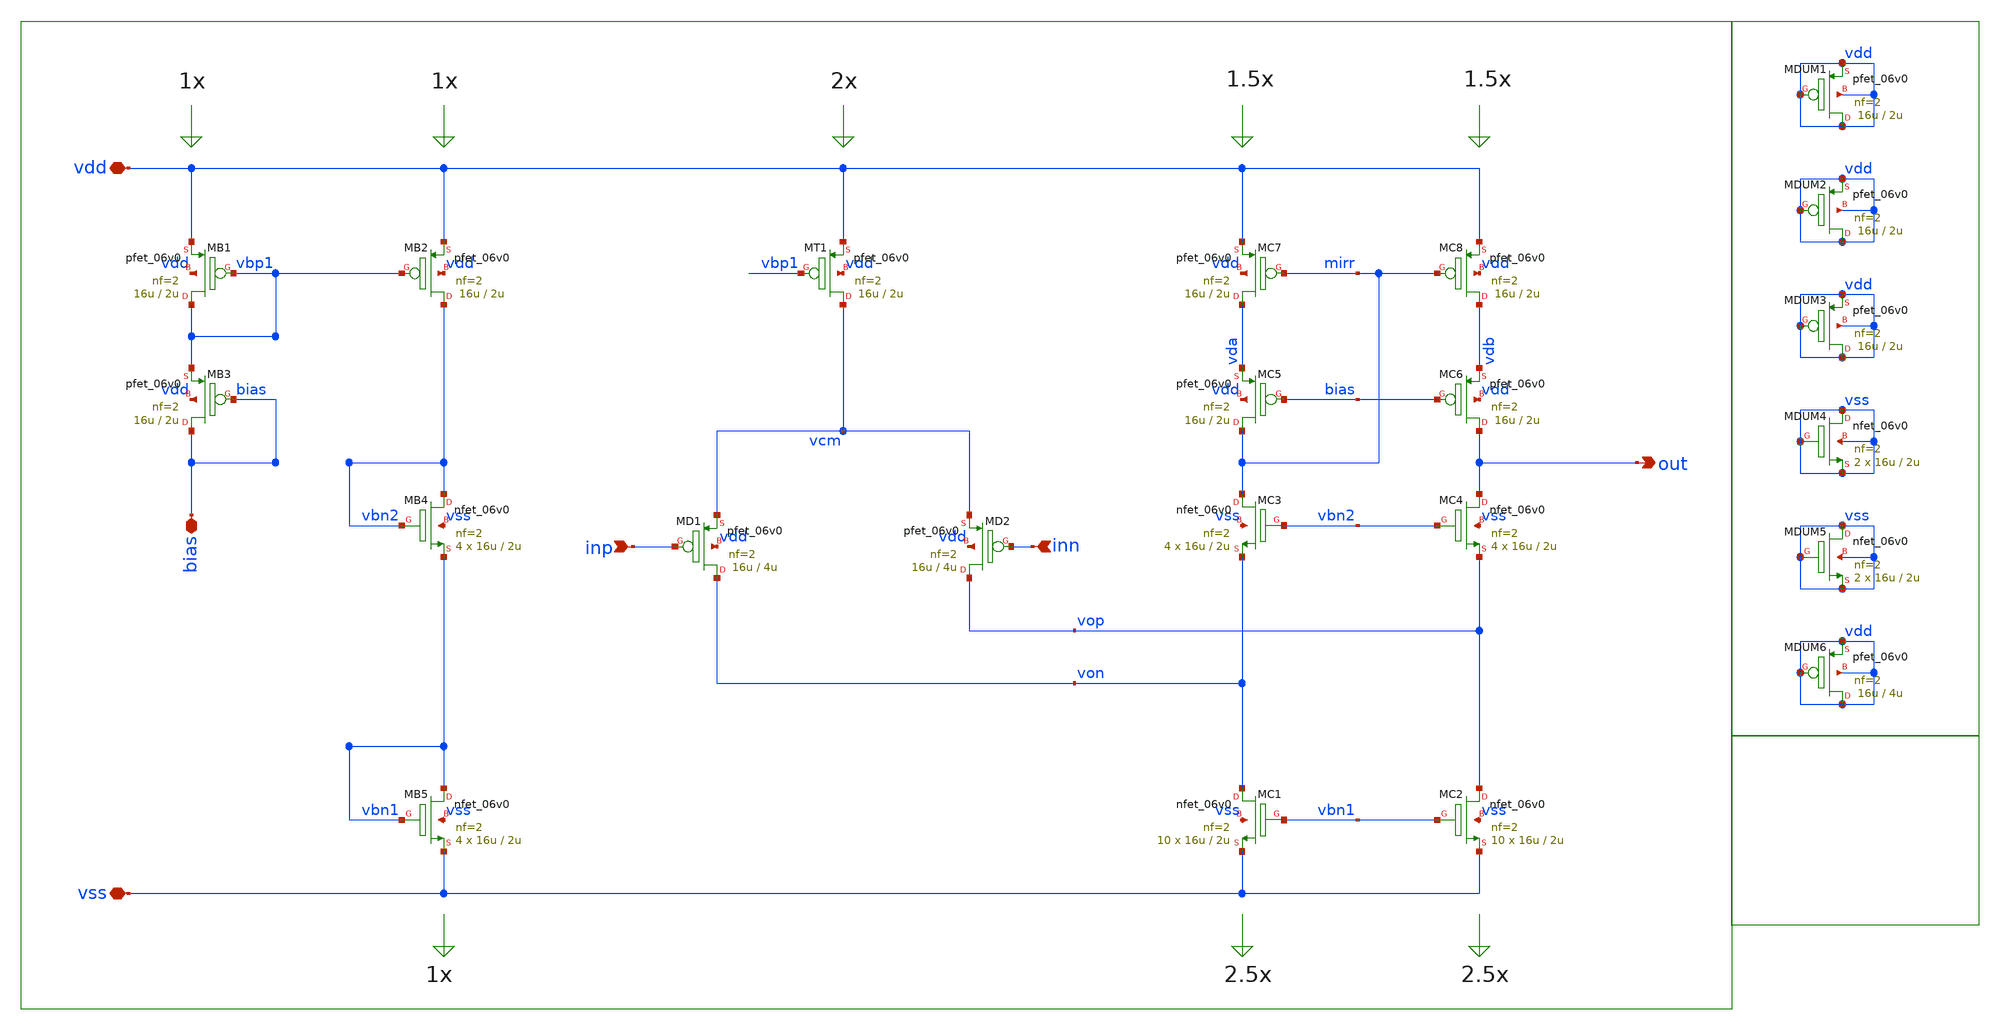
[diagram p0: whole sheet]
** sch_path: xschem/sch/bandgap_cm/bg_amplifier/bg_amplifier.sch
**.subckt bg_amplifier inn inp out bias vdd vss
*.ipin inn
*.ipin inp
*.opin out
*.iopin bias
*.iopin vdd
*.iopin vss
XMB5 vbn1 vbn1 vss vss nfet_06v0 L=2u W=16u nf=2 ad='int((nf+1)/2) * W/nf * 0.18u' as='int((nf+2)/2) * W/nf * 0.18u'
+ pd='2*int((nf+1)/2) * (W/nf + 0.18u)' ps='2*int((nf+2)/2) * (W/nf + 0.18u)' nrd='0.18u / W' nrs='0.18u / W'
+ sa=0 sb=0 sd=0 m=4 par=4
XMC1 von vbn1 vss vss nfet_06v0 L=2u W=16u nf=2 ad='int((nf+1)/2) * W/nf * 0.18u' as='int((nf+2)/2) * W/nf * 0.18u'
+ pd='2*int((nf+1)/2) * (W/nf + 0.18u)' ps='2*int((nf+2)/2) * (W/nf + 0.18u)' nrd='0.18u / W' nrs='0.18u / W'
+ sa=0 sb=0 sd=0 m=10 par=10
XMC2 vop vbn1 vss vss nfet_06v0 L=2u W=16u nf=2 ad='int((nf+1)/2) * W/nf * 0.18u' as='int((nf+2)/2) * W/nf * 0.18u'
+ pd='2*int((nf+1)/2) * (W/nf + 0.18u)' ps='2*int((nf+2)/2) * (W/nf + 0.18u)' nrd='0.18u / W' nrs='0.18u / W'
+ sa=0 sb=0 sd=0 m=10 par=10
XMC3 mirr vbn2 von vss nfet_06v0 L=2u W=16u nf=2 ad='int((nf+1)/2) * W/nf * 0.18u' as='int((nf+2)/2) * W/nf * 0.18u'
+ pd='2*int((nf+1)/2) * (W/nf + 0.18u)' ps='2*int((nf+2)/2) * (W/nf + 0.18u)' nrd='0.18u / W' nrs='0.18u / W'
+ sa=0 sb=0 sd=0 m=4 par=4
XMC4 out vbn2 vop vss nfet_06v0 L=2u W=16u nf=2 ad='int((nf+1)/2) * W/nf * 0.18u' as='int((nf+2)/2) * W/nf * 0.18u'
+ pd='2*int((nf+1)/2) * (W/nf + 0.18u)' ps='2*int((nf+2)/2) * (W/nf + 0.18u)' nrd='0.18u / W' nrs='0.18u / W'
+ sa=0 sb=0 sd=0 m=4 par=4
XMB3 bias bias vbp1 vdd pfet_06v0 L=2u W=16u nf=2 ad='int((nf+1)/2) * W/nf * 0.18u' as='int((nf+2)/2) * W/nf * 0.18u'
+ pd='2*int((nf+1)/2) * (W/nf + 0.18u)' ps='2*int((nf+2)/2) * (W/nf + 0.18u)' nrd='0.18u / W' nrs='0.18u / W'
+ sa=0 sb=0 sd=0 m=2 par=2
XMB1 vbp1 vbp1 vdd vdd pfet_06v0 L=2u W=16u nf=2 ad='int((nf+1)/2) * W/nf * 0.18u' as='int((nf+2)/2) * W/nf * 0.18u'
+ pd='2*int((nf+1)/2) * (W/nf + 0.18u)' ps='2*int((nf+2)/2) * (W/nf + 0.18u)' nrd='0.18u / W' nrs='0.18u / W'
+ sa=0 sb=0 sd=0 m=4 par=4
XMB2 vbn2 vbp1 vdd vdd pfet_06v0 L=2u W=16u nf=2 ad='int((nf+1)/2) * W/nf * 0.18u' as='int((nf+2)/2) * W/nf * 0.18u'
+ pd='2*int((nf+1)/2) * (W/nf + 0.18u)' ps='2*int((nf+2)/2) * (W/nf + 0.18u)' nrd='0.18u / W' nrs='0.18u / W'
+ sa=0 sb=0 sd=0 m=4 par=4
XMT1 vcm vbp1 vdd vdd pfet_06v0 L=2u W=16u nf=2 ad='int((nf+1)/2) * W/nf * 0.18u' as='int((nf+2)/2) * W/nf * 0.18u'
+ pd='2*int((nf+1)/2) * (W/nf + 0.18u)' ps='2*int((nf+2)/2) * (W/nf + 0.18u)' nrd='0.18u / W' nrs='0.18u / W'
+ sa=0 sb=0 sd=0 m=8 par=8
XMD1 von inp vcm vdd pfet_06v0 L=4u W=16u nf=2 ad='int((nf+1)/2) * W/nf * 0.18u' as='int((nf+2)/2) * W/nf * 0.18u'
+ pd='2*int((nf+1)/2) * (W/nf + 0.18u)' ps='2*int((nf+2)/2) * (W/nf + 0.18u)' nrd='0.18u / W' nrs='0.18u / W'
+ sa=0 sb=0 sd=0 m=4 par=4
XMD2 vop inn vcm vdd pfet_06v0 L=4u W=16u nf=2 ad='int((nf+1)/2) * W/nf * 0.18u' as='int((nf+2)/2) * W/nf * 0.18u'
+ pd='2*int((nf+1)/2) * (W/nf + 0.18u)' ps='2*int((nf+2)/2) * (W/nf + 0.18u)' nrd='0.18u / W' nrs='0.18u / W'
+ sa=0 sb=0 sd=0 m=4 par=4
XMC7 vda mirr vdd vdd pfet_06v0 L=2u W=16u nf=2 ad='int((nf+1)/2) * W/nf * 0.18u' as='int((nf+2)/2) * W/nf * 0.18u'
+ pd='2*int((nf+1)/2) * (W/nf + 0.18u)' ps='2*int((nf+2)/2) * (W/nf + 0.18u)' nrd='0.18u / W' nrs='0.18u / W'
+ sa=0 sb=0 sd=0 m=2 par=2
XMC8 vdb mirr vdd vdd pfet_06v0 L=2u W=16u nf=2 ad='int((nf+1)/2) * W/nf * 0.18u' as='int((nf+2)/2) * W/nf * 0.18u'
+ pd='2*int((nf+1)/2) * (W/nf + 0.18u)' ps='2*int((nf+2)/2) * (W/nf + 0.18u)' nrd='0.18u / W' nrs='0.18u / W'
+ sa=0 sb=0 sd=0 m=2 par=2
XMC5 mirr bias vda vdd pfet_06v0 L=2u W=16u nf=2 ad='int((nf+1)/2) * W/nf * 0.18u' as='int((nf+2)/2) * W/nf * 0.18u'
+ pd='2*int((nf+1)/2) * (W/nf + 0.18u)' ps='2*int((nf+2)/2) * (W/nf + 0.18u)' nrd='0.18u / W' nrs='0.18u / W'
+ sa=0 sb=0 sd=0 m=4 par=4
XMC6 out bias vdb vdd pfet_06v0 L=2u W=16u nf=2 ad='int((nf+1)/2) * W/nf * 0.18u' as='int((nf+2)/2) * W/nf * 0.18u'
+ pd='2*int((nf+1)/2) * (W/nf + 0.18u)' ps='2*int((nf+2)/2) * (W/nf + 0.18u)' nrd='0.18u / W' nrs='0.18u / W'
+ sa=0 sb=0 sd=0 m=4 par=4
XMB4 vbn2 vbn2 vbn1 vss nfet_06v0 L=2u W=16u nf=2 ad='int((nf+1)/2) * W/nf * 0.18u' as='int((nf+2)/2) * W/nf * 0.18u'
+ pd='2*int((nf+1)/2) * (W/nf + 0.18u)' ps='2*int((nf+2)/2) * (W/nf + 0.18u)' nrd='0.18u / W' nrs='0.18u / W'
+ sa=0 sb=0 sd=0 m=4 par=4
XMDUM1 vdd vdd vdd vdd pfet_06v0 L=2u W=16u nf=2 ad='int((nf+1)/2) * W/nf * 0.18u' as='int((nf+2)/2) * W/nf * 0.18u'
+ pd='2*int((nf+1)/2) * (W/nf + 0.18u)' ps='2*int((nf+2)/2) * (W/nf + 0.18u)' nrd='0.18u / W' nrs='0.18u / W'
+ sa=0 sb=0 sd=0 m=4 par=4
XMDUM2 vdd vdd vdd vdd pfet_06v0 L=2u W=16u nf=2 ad='int((nf+1)/2) * W/nf * 0.18u' as='int((nf+2)/2) * W/nf * 0.18u'
+ pd='2*int((nf+1)/2) * (W/nf + 0.18u)' ps='2*int((nf+2)/2) * (W/nf + 0.18u)' nrd='0.18u / W' nrs='0.18u / W'
+ sa=0 sb=0 sd=0 m=4 par=4
XMDUM3 vdd vdd vdd vdd pfet_06v0 L=2u W=16u nf=2 ad='int((nf+1)/2) * W/nf * 0.18u' as='int((nf+2)/2) * W/nf * 0.18u'
+ pd='2*int((nf+1)/2) * (W/nf + 0.18u)' ps='2*int((nf+2)/2) * (W/nf + 0.18u)' nrd='0.18u / W' nrs='0.18u / W'
+ sa=0 sb=0 sd=0 m=2 par=2
XMDUM4 vss vss vss vss nfet_06v0 L=2u W=16u nf=2 ad='int((nf+1)/2) * W/nf * 0.18u' as='int((nf+2)/2) * W/nf * 0.18u'
+ pd='2*int((nf+1)/2) * (W/nf + 0.18u)' ps='2*int((nf+2)/2) * (W/nf + 0.18u)' nrd='0.18u / W' nrs='0.18u / W'
+ sa=0 sb=0 sd=0 m=2 par=2
XMDUM5 vss vss vss vss nfet_06v0 L=2u W=16u nf=2 ad='int((nf+1)/2) * W/nf * 0.18u' as='int((nf+2)/2) * W/nf * 0.18u'
+ pd='2*int((nf+1)/2) * (W/nf + 0.18u)' ps='2*int((nf+2)/2) * (W/nf + 0.18u)' nrd='0.18u / W' nrs='0.18u / W'
+ sa=0 sb=0 sd=0 m=2 par=2
XMDUM6 vdd vdd vdd vdd pfet_06v0 L=4u W=16u nf=2 ad='int((nf+1)/2) * W/nf * 0.18u' as='int((nf+2)/2) * W/nf * 0.18u'
+ pd='2*int((nf+1)/2) * (W/nf + 0.18u)' ps='2*int((nf+2)/2) * (W/nf + 0.18u)' nrd='0.18u / W' nrs='0.18u / W'
+ sa=0 sb=0 sd=0 m=16 par=16
**.ends
.end
